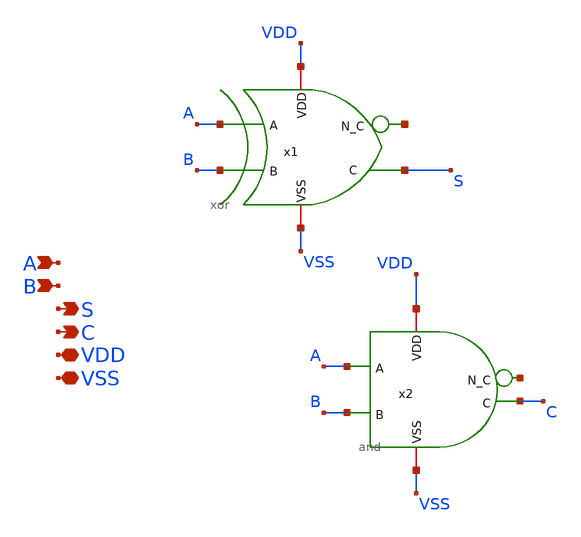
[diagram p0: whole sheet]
** sch_path: schematics/components/half-adder/half-adder.sch
**.subckt half-adder A B S C VDD VSS
*.ipin A
*.ipin B
*.opin S
*.opin C
*.iopin VDD
*.iopin VSS
x1 A B net1 S VDD VSS xor
x2 A B net2 C VDD VSS and
**.ends

* expanding   symbol:  schematics/logic-gates/xor/xor.sym # of pins=6
** sym_path: schematics/logic-gates/xor/xor.sym
** sch_path: schematics/logic-gates/xor/xor.sch
.subckt xor A B N_C C VDD VSS
*.ipin A
*.ipin B
*.opin C
*.opin N_C
*.iopin VDD
*.iopin VSS
XM1 N_A A VSS VSS nfet_03v3 L=0.28u W=0.22u nf=1 ad='int((nf+1)/2) * W/nf * 0.18u' as='int((nf+2)/2) * W/nf * 0.18u'
+ pd='2*int((nf+1)/2) * (W/nf + 0.18u)' ps='2*int((nf+2)/2) * (W/nf + 0.18u)' nrd='0.18u / W' nrs='0.18u / W'
+ sa=0 sb=0 sd=0 m=1
XM2 N_A A VDD VDD pfet_03v3 L=0.28u W=0.22u nf=1 ad='int((nf+1)/2) * W/nf * 0.18u' as='int((nf+2)/2) * W/nf * 0.18u'
+ pd='2*int((nf+1)/2) * (W/nf + 0.18u)' ps='2*int((nf+2)/2) * (W/nf + 0.18u)' nrd='0.18u / W' nrs='0.18u / W'
+ sa=0 sb=0 sd=0 m=1
XM3 N_B B VDD VDD pfet_03v3 L=0.28u W=0.22u nf=1 ad='int((nf+1)/2) * W/nf * 0.18u' as='int((nf+2)/2) * W/nf * 0.18u'
+ pd='2*int((nf+1)/2) * (W/nf + 0.18u)' ps='2*int((nf+2)/2) * (W/nf + 0.18u)' nrd='0.18u / W' nrs='0.18u / W'
+ sa=0 sb=0 sd=0 m=1
XM4 N_B B VSS VSS nfet_03v3 L=0.28u W=0.22u nf=1 ad='int((nf+1)/2) * W/nf * 0.18u' as='int((nf+2)/2) * W/nf * 0.18u'
+ pd='2*int((nf+1)/2) * (W/nf + 0.18u)' ps='2*int((nf+2)/2) * (W/nf + 0.18u)' nrd='0.18u / W' nrs='0.18u / W'
+ sa=0 sb=0 sd=0 m=1
XM5 net2 B VSS VSS nfet_03v3 L=0.28u W=0.22u nf=1 ad='int((nf+1)/2) * W/nf * 0.18u' as='int((nf+2)/2) * W/nf * 0.18u'
+ pd='2*int((nf+1)/2) * (W/nf + 0.18u)' ps='2*int((nf+2)/2) * (W/nf + 0.18u)' nrd='0.18u / W' nrs='0.18u / W'
+ sa=0 sb=0 sd=0 m=1
XM6 net3 N_B VSS VSS nfet_03v3 L=0.28u W=0.22u nf=1 ad='int((nf+1)/2) * W/nf * 0.18u' as='int((nf+2)/2) * W/nf * 0.18u'
+ pd='2*int((nf+1)/2) * (W/nf + 0.18u)' ps='2*int((nf+2)/2) * (W/nf + 0.18u)' nrd='0.18u / W' nrs='0.18u / W'
+ sa=0 sb=0 sd=0 m=1
XM7 C A net2 VSS nfet_03v3 L=0.28u W=0.22u nf=1 ad='int((nf+1)/2) * W/nf * 0.18u' as='int((nf+2)/2) * W/nf * 0.18u'
+ pd='2*int((nf+1)/2) * (W/nf + 0.18u)' ps='2*int((nf+2)/2) * (W/nf + 0.18u)' nrd='0.18u / W' nrs='0.18u / W'
+ sa=0 sb=0 sd=0 m=1
XM8 C N_A net3 VSS nfet_03v3 L=0.28u W=0.22u nf=1 ad='int((nf+1)/2) * W/nf * 0.18u' as='int((nf+2)/2) * W/nf * 0.18u'
+ pd='2*int((nf+1)/2) * (W/nf + 0.18u)' ps='2*int((nf+2)/2) * (W/nf + 0.18u)' nrd='0.18u / W' nrs='0.18u / W'
+ sa=0 sb=0 sd=0 m=1
XM9 C B net1 VDD pfet_03v3 L=0.28u W=0.22u nf=1 ad='int((nf+1)/2) * W/nf * 0.18u' as='int((nf+2)/2) * W/nf * 0.18u'
+ pd='2*int((nf+1)/2) * (W/nf + 0.18u)' ps='2*int((nf+2)/2) * (W/nf + 0.18u)' nrd='0.18u / W' nrs='0.18u / W'
+ sa=0 sb=0 sd=0 m=1
XM10 C N_B net4 VDD pfet_03v3 L=0.28u W=0.22u nf=1 ad='int((nf+1)/2) * W/nf * 0.18u' as='int((nf+2)/2) * W/nf * 0.18u'
+ pd='2*int((nf+1)/2) * (W/nf + 0.18u)' ps='2*int((nf+2)/2) * (W/nf + 0.18u)' nrd='0.18u / W' nrs='0.18u / W'
+ sa=0 sb=0 sd=0 m=1
XM11 net1 N_A VDD VDD pfet_03v3 L=0.28u W=0.22u nf=1 ad='int((nf+1)/2) * W/nf * 0.18u' as='int((nf+2)/2) * W/nf * 0.18u'
+ pd='2*int((nf+1)/2) * (W/nf + 0.18u)' ps='2*int((nf+2)/2) * (W/nf + 0.18u)' nrd='0.18u / W' nrs='0.18u / W'
+ sa=0 sb=0 sd=0 m=1
XM12 net4 A VDD VDD pfet_03v3 L=0.28u W=0.22u nf=1 ad='int((nf+1)/2) * W/nf * 0.18u' as='int((nf+2)/2) * W/nf * 0.18u'
+ pd='2*int((nf+1)/2) * (W/nf + 0.18u)' ps='2*int((nf+2)/2) * (W/nf + 0.18u)' nrd='0.18u / W' nrs='0.18u / W'
+ sa=0 sb=0 sd=0 m=1
XM13 N_C C VDD VDD pfet_03v3 L=0.28u W=0.22u nf=1 ad='int((nf+1)/2) * W/nf * 0.18u' as='int((nf+2)/2) * W/nf * 0.18u'
+ pd='2*int((nf+1)/2) * (W/nf + 0.18u)' ps='2*int((nf+2)/2) * (W/nf + 0.18u)' nrd='0.18u / W' nrs='0.18u / W'
+ sa=0 sb=0 sd=0 m=1
XM14 N_C C VSS VSS nfet_03v3 L=0.28u W=0.22u nf=1 ad='int((nf+1)/2) * W/nf * 0.18u' as='int((nf+2)/2) * W/nf * 0.18u'
+ pd='2*int((nf+1)/2) * (W/nf + 0.18u)' ps='2*int((nf+2)/2) * (W/nf + 0.18u)' nrd='0.18u / W' nrs='0.18u / W'
+ sa=0 sb=0 sd=0 m=1
.ends


* expanding   symbol:  schematics/logic-gates/and/and.sym # of pins=6
** sym_path: schematics/logic-gates/and/and.sym
** sch_path: schematics/logic-gates/and/and.sch
.subckt and A B N_C C VDD VSS
*.ipin A
*.ipin B
*.opin C
*.opin N_C
*.iopin VDD
*.iopin VSS
XM1 N_C B net1 VSS nfet_03v3 L=0.28u W=0.22u nf=1 ad='int((nf+1)/2) * W/nf * 0.18u' as='int((nf+2)/2) * W/nf * 0.18u'
+ pd='2*int((nf+1)/2) * (W/nf + 0.18u)' ps='2*int((nf+2)/2) * (W/nf + 0.18u)' nrd='0.18u / W' nrs='0.18u / W'
+ sa=0 sb=0 sd=0 m=1
XM2 N_C A VDD VDD pfet_03v3 L=0.28u W=0.22u nf=1 ad='int((nf+1)/2) * W/nf * 0.18u' as='int((nf+2)/2) * W/nf * 0.18u'
+ pd='2*int((nf+1)/2) * (W/nf + 0.18u)' ps='2*int((nf+2)/2) * (W/nf + 0.18u)' nrd='0.18u / W' nrs='0.18u / W'
+ sa=0 sb=0 sd=0 m=1
XM3 N_C B VDD VDD pfet_03v3 L=0.28u W=0.22u nf=1 ad='int((nf+1)/2) * W/nf * 0.18u' as='int((nf+2)/2) * W/nf * 0.18u'
+ pd='2*int((nf+1)/2) * (W/nf + 0.18u)' ps='2*int((nf+2)/2) * (W/nf + 0.18u)' nrd='0.18u / W' nrs='0.18u / W'
+ sa=0 sb=0 sd=0 m=1
XM4 net1 A VSS VSS nfet_03v3 L=0.28u W=0.22u nf=1 ad='int((nf+1)/2) * W/nf * 0.18u' as='int((nf+2)/2) * W/nf * 0.18u'
+ pd='2*int((nf+1)/2) * (W/nf + 0.18u)' ps='2*int((nf+2)/2) * (W/nf + 0.18u)' nrd='0.18u / W' nrs='0.18u / W'
+ sa=0 sb=0 sd=0 m=1
XM5 C N_C VDD VDD pfet_03v3 L=0.28u W=0.22u nf=1 ad='int((nf+1)/2) * W/nf * 0.18u' as='int((nf+2)/2) * W/nf * 0.18u'
+ pd='2*int((nf+1)/2) * (W/nf + 0.18u)' ps='2*int((nf+2)/2) * (W/nf + 0.18u)' nrd='0.18u / W' nrs='0.18u / W'
+ sa=0 sb=0 sd=0 m=1
XM6 C N_C VSS VSS nfet_03v3 L=0.28u W=0.22u nf=1 ad='int((nf+1)/2) * W/nf * 0.18u' as='int((nf+2)/2) * W/nf * 0.18u'
+ pd='2*int((nf+1)/2) * (W/nf + 0.18u)' ps='2*int((nf+2)/2) * (W/nf + 0.18u)' nrd='0.18u / W' nrs='0.18u / W'
+ sa=0 sb=0 sd=0 m=1
.ends

.end
